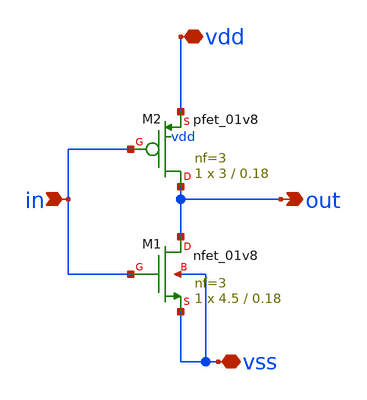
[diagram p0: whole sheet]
** sch_path: Lab1_inverter/xschem/inverter.sch
**.subckt inverter in out vdd vss
*.ipin in
*.opin out
*.iopin vdd
*.iopin vss
XM1 out in vss vss sky130_fd_pr__nfet_01v8 L=0.18 W=4.5 nf=3 ad='int((nf + 1)/2) * W / nf * 0.29' as='int((nf + 2)/2) * W / nf * 0.29'
+ pd='2*int((nf + 1)/2) * (W / nf + 0.29)' ps='2*int((nf + 2)/2) * (W / nf + 0.29)' nrd='0.29 / W ' nrs='0.29 / W '
+ sa=0 sb=0 sd=0 mult=1 m=1
XM2 out in vdd vdd sky130_fd_pr__pfet_01v8 L=0.18 W=3 nf=3 ad='int((nf + 1)/2) * W / nf * 0.29' as='int((nf + 2)/2) * W / nf * 0.29'
+ pd='2*int((nf + 1)/2) * (W / nf + 0.29)' ps='2*int((nf + 2)/2) * (W / nf + 0.29)' nrd='0.29 / W ' nrs='0.29 / W '
+ sa=0 sb=0 sd=0 mult=1 m=1
**.ends
.end
